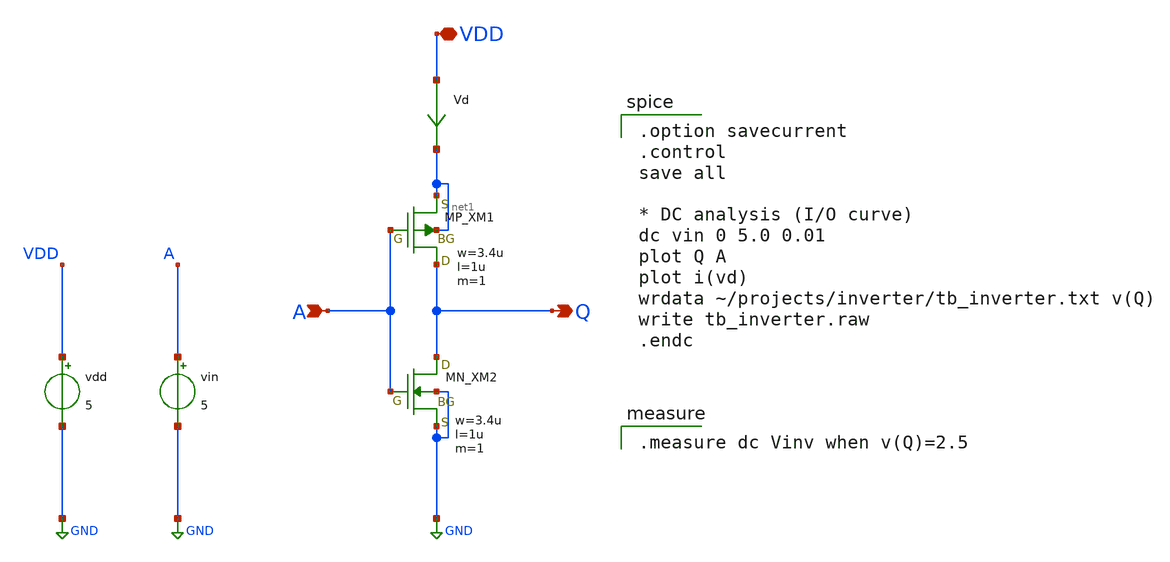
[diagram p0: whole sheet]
** sch_path: member_project/inverter/ichiken/TadasukeKuramochi/tb_inverter_TadasukeKuramochi.sch
**.subckt tb_inverter_TadasukeKuramochi A Q VDD
*.ipin A
*.opin Q
*.iopin VDD
XXM1 Q A net1 net1 PMOS w=3.4u l=1u as=0 ad=0 ps=0 pd=0 nrd=0 nrs=0 m=1
XXM2 Q A GND GND NMOS w=3.4u l=1u as=0 ad=0 ps=0 pd=0 nrd=0 nrs=0 m=1
vin A GND 5
vdd VDD GND 5
Vd VDD net1 0
.save i(vd)
**** begin user architecture code
 .include $::LIB/ip62_models

.option savecurrent
.control
save all

* DC analysis (I/O curve)
dc vin 0 5.0 0.01
plot Q A
plot i(vd)
wrdata ~/projects/inverter/tb_inverter.txt v(Q)
write tb_inverter.raw
.endc


.measure dc Vinv when v(Q)=2.5

**** end user architecture code
**.ends
.GLOBAL GND
.end
